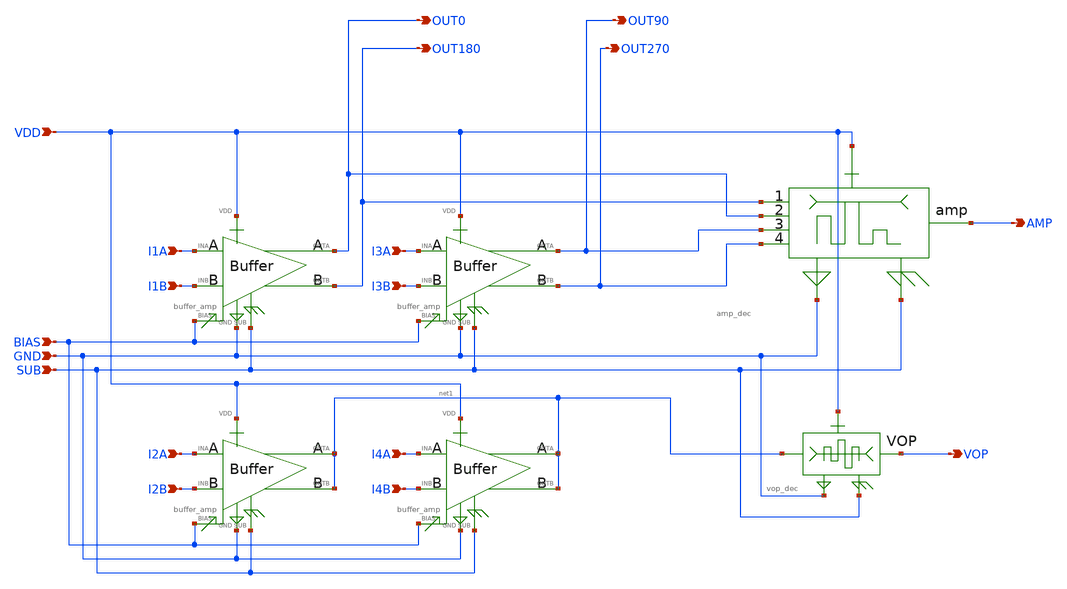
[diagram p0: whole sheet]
** sch_path: design/vco/1.7G~10G/schematic/buffer_amp_vop.sch
**.subckt buffer_amp_vop BIAS GND SUB I1A I1B I2A I2B I3A I3B I4A I4B VDD AMP VOP OUT0 OUT180 OUT90
*+ OUT270
*.ipin BIAS
*.ipin GND
*.ipin SUB
*.ipin I1A
*.ipin I1B
*.ipin I2A
*.ipin I2B
*.ipin I3A
*.ipin I3B
*.ipin I4A
*.ipin I4B
*.ipin VDD
*.opin AMP
*.opin VOP
*.opin OUT0
*.opin OUT180
*.opin OUT90
*.opin OUT270
X2 I2A I2B BIAS VDD GND SUB net1 net1 buffer_amp
X4 I4A I4B BIAS VDD GND SUB net1 net1 buffer_amp
X1 I1A I1B BIAS VDD GND SUB OUT0 OUT180 buffer_amp
X3 I3A I3B BIAS VDD GND SUB OUT90 OUT270 buffer_amp
X5 OUT180 OUT0 OUT90 OUT270 AMP VDD GND SUB amp_dec
X6 net1 VDD GND SUB VOP vop_dec
**.ends
.end
